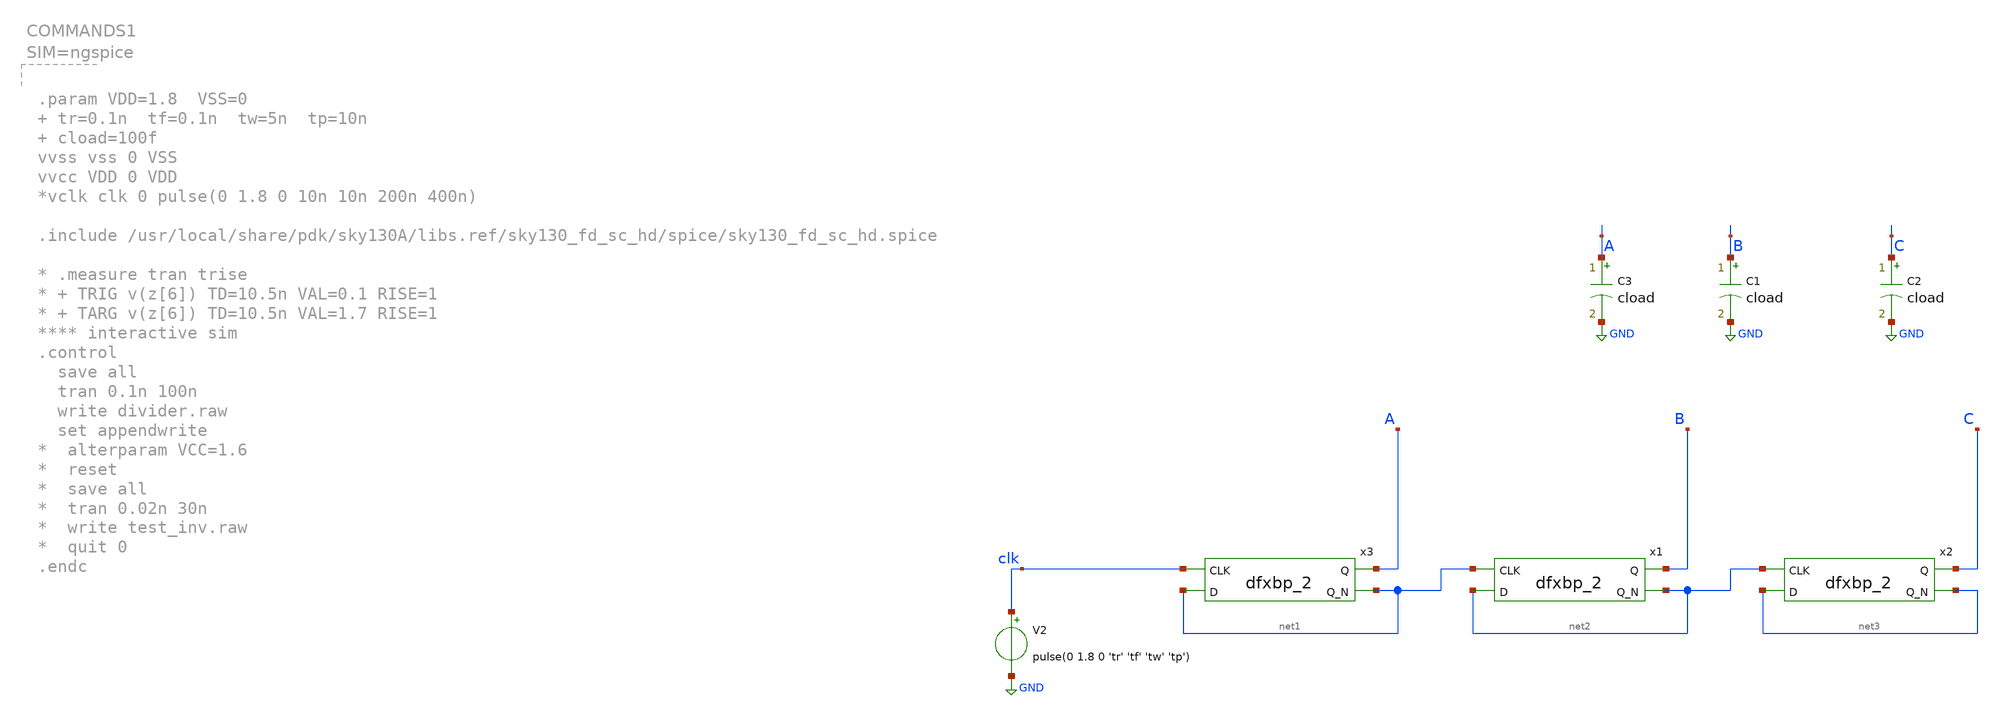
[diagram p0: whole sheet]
** sch_path: xschem01/divider/divider.sch
.lib $::SKYWATER_MODELS/sky130.lib.spice tt
.include $::SKYWATER_STDCELLS/sky130_fd_sc_hd.spice

**.subckt divider
x3 clk net1 VSS VSS VDD VDD A net1 sky130_fd_sc_hd__dfxbp_2
V2 clk GND pulse(0 1.8 0 'tr' 'tf' 'tw' 'tp')
x1 net1 net2 VSS VSS VDD VDD B net2 sky130_fd_sc_hd__dfxbp_2
x2 net2 net3 VSS VSS VDD VDD C net3 sky130_fd_sc_hd__dfxbp_2
C3 A GND cload m=1
C1 B GND cload m=1
C2 C GND cload m=1
**** begin user architecture code



.param VDD=1.8  VSS=0  tr=0.1n  tf=0.1n  tw=5n  tp=10n  cload=100f
vvss vss 0 VSS
vvcc VDD 0 VDD
*vclk clk 0 pulse(0 1.8 0 10n 10n 200n 400n)

.include /usr/local/share/pdk/sky130A/libs.ref/sky130_fd_sc_hd/spice/sky130_fd_sc_hd.spice

* .measure tran trise
* + TRIG v(z[6]) TD=10.5n VAL=0.1 RISE=1
* + TARG v(z[6]) TD=10.5n VAL=1.7 RISE=1
**** interactive sim
.control
  save all
  tran 0.1n 100n
  let power= i(vvcc)*v(vdd,vss)
  meas tran power_avg  avg  power  from=1n  to=90n
  meas tran power_rms  rms  power  from=1n  to=90n
  write divider.raw
  set appendwrite
*  alterparam VCC=1.6
*  reset
*  save all
*  tran 0.02n 30n
*  write test_inv.raw
*  quit 0
.endc



**** end user architecture code
**.ends
.GLOBAL GND
.end
